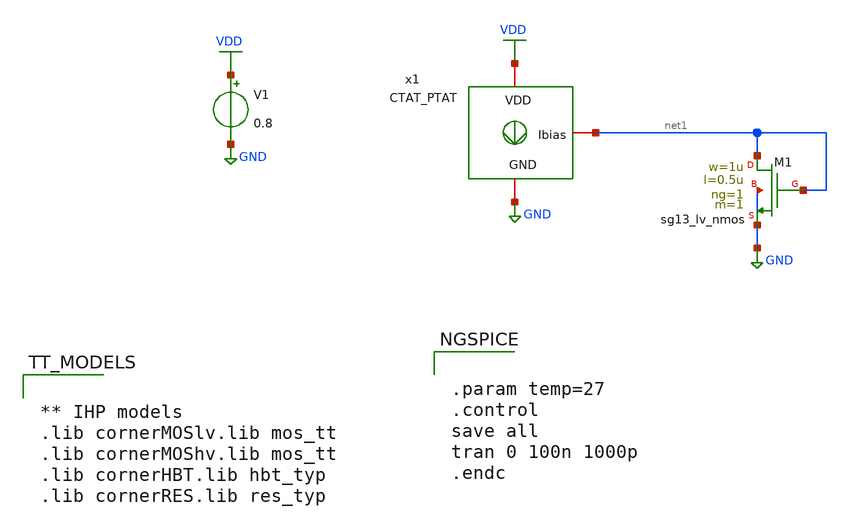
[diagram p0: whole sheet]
** sch_path: SSDOR_1V_v1/components/Ib_4u/CTAT_PTAT/tb_CTAT_PTAT.sch
**.subckt tb_CTAT_PTAT
V1 VDD GND 0.8
XM1 net1 net1 GND GND sg13_lv_nmos w=1u l=0.5u ng=1 m=1 mm_ok=1
x1 VDD net1 GND CTAT_PTAT
**** begin user architecture code


** IHP models
.lib cornerMOSlv.lib mos_tt
.lib cornerMOShv.lib mos_tt
.lib cornerHBT.lib hbt_typ
.lib cornerRES.lib res_typ




.param temp=27
.control
save all
tran 0 100n 1000p
.endc


**** end user architecture code
**.ends
.GLOBAL VDD
.GLOBAL GND
.end
